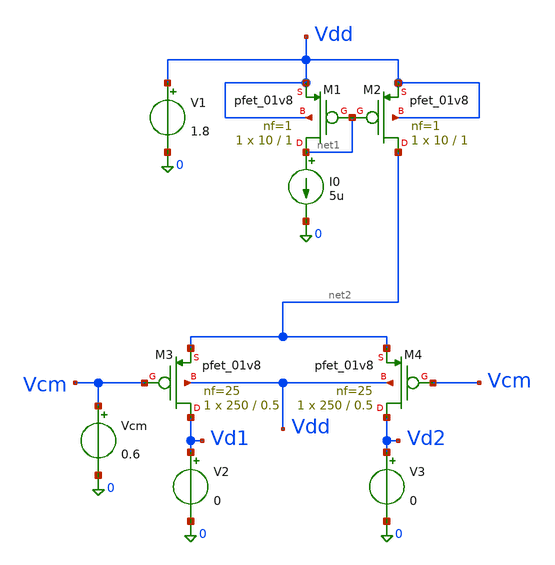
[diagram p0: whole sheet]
** sch_path: stage1/schematics/mirror_and_diff_pair.sch
**.subckt mirror_and_diff_pair
I0 net1 0 5u
XM1 net1 net1 Vdd Vdd sky130_fd_pr__pfet_01v8 L=1 W=10 nf=1 ad='int((1 + 1)/2) * 10 / 1 * 0.29' as='int((1 + 2)/2) * 10 / 1 * 0.29'
+ pd='2*int((1 + 1)/2) * (10 / 1 + 0.29)' ps='2*int((1 + 2)/2) * (10 / 1 + 0.29)' nrd='0.29 / 10 ' nrs='0.29 / 10 '
+ sa=0 sb=0 sd=0 mult=1 m=1
XM2 net2 net1 Vdd Vdd sky130_fd_pr__pfet_01v8 L=1 W=10 nf=1 ad='int((1 + 1)/2) * 10 / 1 * 0.29' as='int((1 + 2)/2) * 10 / 1 * 0.29'
+ pd='2*int((1 + 1)/2) * (10 / 1 + 0.29)' ps='2*int((1 + 2)/2) * (10 / 1 + 0.29)' nrd='0.29 / 10 ' nrs='0.29 / 10 '
+ sa=0 sb=0 sd=0 mult=1 m=1
V1 Vdd 0 1.8
XM3 Vd1 Vcm net2 Vdd sky130_fd_pr__pfet_01v8 L=0.5 W=250 nf=25 ad='int((25 + 1)/2) * 250 / 25 * 0.29'
+ as='int((25 + 2)/2) * 250 / 25 * 0.29' pd='2*int((25 + 1)/2) * (250 / 25 + 0.29)' ps='2*int((25 + 2)/2) * (250 / 25 + 0.29)'
+ nrd='0.29 / 250 ' nrs='0.29 / 250 ' sa=0 sb=0 sd=0 mult=1 m=1
XM4 Vd2 Vcm net2 Vdd sky130_fd_pr__pfet_01v8 L=0.5 W=250 nf=25 ad='int((25 + 1)/2) * 250 / 25 * 0.29'
+ as='int((25 + 2)/2) * 250 / 25 * 0.29' pd='2*int((25 + 1)/2) * (250 / 25 + 0.29)' ps='2*int((25 + 2)/2) * (250 / 25 + 0.29)'
+ nrd='0.29 / 250 ' nrs='0.29 / 250 ' sa=0 sb=0 sd=0 mult=1 m=1
V2 Vd1 0 0
V3 Vd2 0 0
Vcm Vcm 0 0.6
**** begin user architecture code

** opencircuitdesign pdks install
.lib $::SKYWATER_MODELS/sky130.lib.spice tt


.include mirror_and_diff_pair.save
.options savecurrents

.control
	save all
	dc Vcm 0 1.8 0.01
	let i_mirror = V2#branch + V3#branch
	plot i_mirror vs Vcm
.endc

**** end user architecture code
**.ends
.end
